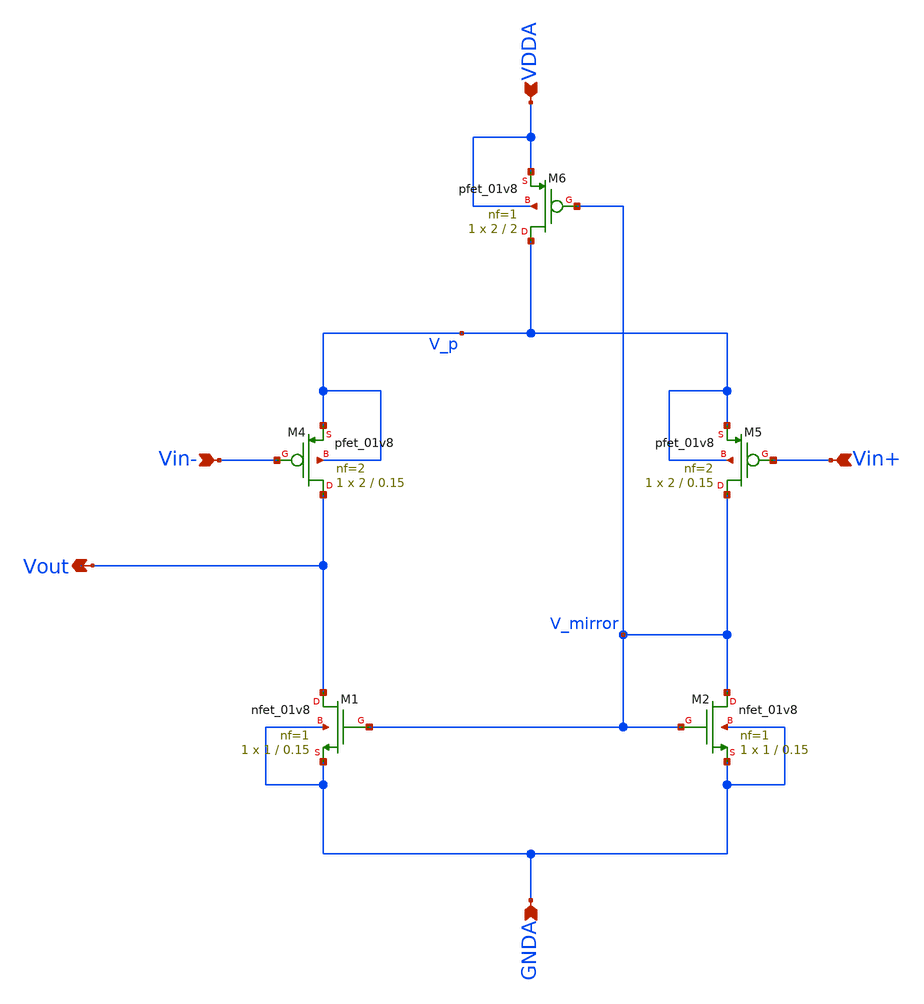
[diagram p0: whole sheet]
** sch_path: projects/bandgapref/xschem_ngspice/new_files/opamp_bandgap_3.sch
**.subckt opamp_bandgap_3 Vin+ Vout Vin- GNDA VDDA
*.ipin Vin+
*.opin Vout
*.ipin Vin-
*.ipin GNDA
*.ipin VDDA
XM1 Vout V_mirror GNDA GNDA sky130_fd_pr__nfet_01v8 L=0.15 W=1 nf=1 ad='int((nf+1)/2) * W/nf * 0.29'
+ as='int((nf+2)/2) * W/nf * 0.29' pd='2*int((nf+1)/2) * (W/nf + 0.29)' ps='2*int((nf+2)/2) * (W/nf + 0.29)'
+ nrd='0.29 / W' nrs='0.29 / W' sa=0 sb=0 sd=0 mult=1 m=1
XM2 V_mirror V_mirror GNDA GNDA sky130_fd_pr__nfet_01v8 L=0.15 W=1 nf=1 ad='int((nf+1)/2) * W/nf * 0.29'
+ as='int((nf+2)/2) * W/nf * 0.29' pd='2*int((nf+1)/2) * (W/nf + 0.29)' ps='2*int((nf+2)/2) * (W/nf + 0.29)'
+ nrd='0.29 / W' nrs='0.29 / W' sa=0 sb=0 sd=0 mult=1 m=1
XM4 Vout Vin- V_p V_p sky130_fd_pr__pfet_01v8 L=0.15 W=2 nf=2 ad='int((nf+1)/2) * W/nf * 0.29' as='int((nf+2)/2) * W/nf * 0.29'
+ pd='2*int((nf+1)/2) * (W/nf + 0.29)' ps='2*int((nf+2)/2) * (W/nf + 0.29)' nrd='0.29 / W' nrs='0.29 / W'
+ sa=0 sb=0 sd=0 mult=1 m=1
XM5 V_mirror Vin+ V_p V_p sky130_fd_pr__pfet_01v8 L=0.15 W=2 nf=2 ad='int((nf+1)/2) * W/nf * 0.29' as='int((nf+2)/2) * W/nf * 0.29'
+ pd='2*int((nf+1)/2) * (W/nf + 0.29)' ps='2*int((nf+2)/2) * (W/nf + 0.29)' nrd='0.29 / W' nrs='0.29 / W'
+ sa=0 sb=0 sd=0 mult=1 m=1
XM6 V_p V_mirror VDDA VDDA sky130_fd_pr__pfet_01v8 L=2 W=2 nf=1 ad='int((nf+1)/2) * W/nf * 0.29' as='int((nf+2)/2) * W/nf * 0.29'
+ pd='2*int((nf+1)/2) * (W/nf + 0.29)' ps='2*int((nf+2)/2) * (W/nf + 0.29)' nrd='0.29 / W' nrs='0.29 / W'
+ sa=0 sb=0 sd=0 mult=1 m=1
**.ends
.end
